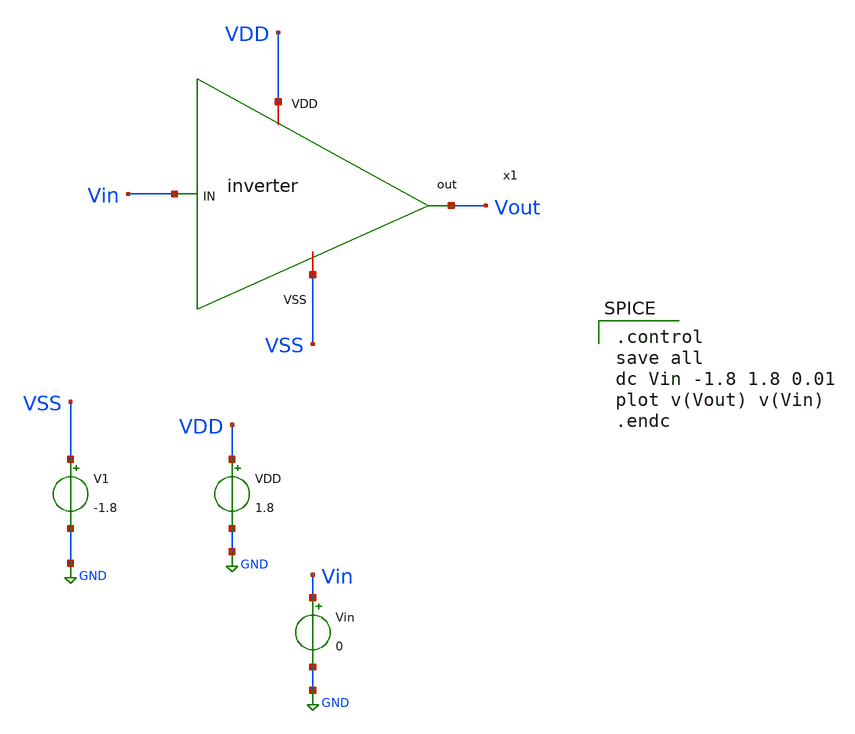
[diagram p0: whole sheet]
** sch_path: new_tb_inverter.sch
**.subckt new_tb_inverter
VDD VDD GND 1.8
Vin Vin GND 0
V1 VSS GND -1.8
x1 VDD Vin Vout VSS inverter
**** begin user architecture code

.lib /home/ttuser/pdk/sky130A/libs.tech/combined/sky130.lib.spice tt


.control
save all
dc Vin -1.8 1.8 0.01
plot v(Vout) v(Vin)
.endc


**** end user architecture code
**.ends

* expanding   symbol:  /home/ttuser/Documents/ADCAnalogDesign/inverter.sym # of pins=4
** sym_path: inverter.sym
** sch_path: inverter.sch
.subckt inverter VDD IN out VSS
*.ipin IN
*.opin out
*.iopin VDD
*.iopin VSS
XM3 out IN VDD VDD sky130_fd_pr__pfet_01v8 L=0.15 W=1 nf=1 ad='int((nf+1)/2) * W/nf * 0.29' as='int((nf+2)/2) * W/nf * 0.29'
+ pd='2*int((nf+1)/2) * (W/nf + 0.29)' ps='2*int((nf+2)/2) * (W/nf + 0.29)' nrd='0.29 / W' nrs='0.29 / W'
+ sa=0 sb=0 sd=0 mult=1 m=1
XM2 out IN VSS VSS sky130_fd_pr__nfet_01v8 L=0.15 W=1 nf=1 ad='int((nf+1)/2) * W/nf * 0.29' as='int((nf+2)/2) * W/nf * 0.29'
+ pd='2*int((nf+1)/2) * (W/nf + 0.29)' ps='2*int((nf+2)/2) * (W/nf + 0.29)' nrd='0.29 / W' nrs='0.29 / W'
+ sa=0 sb=0 sd=0 mult=1 m=1
.ends

.GLOBAL GND
.end
